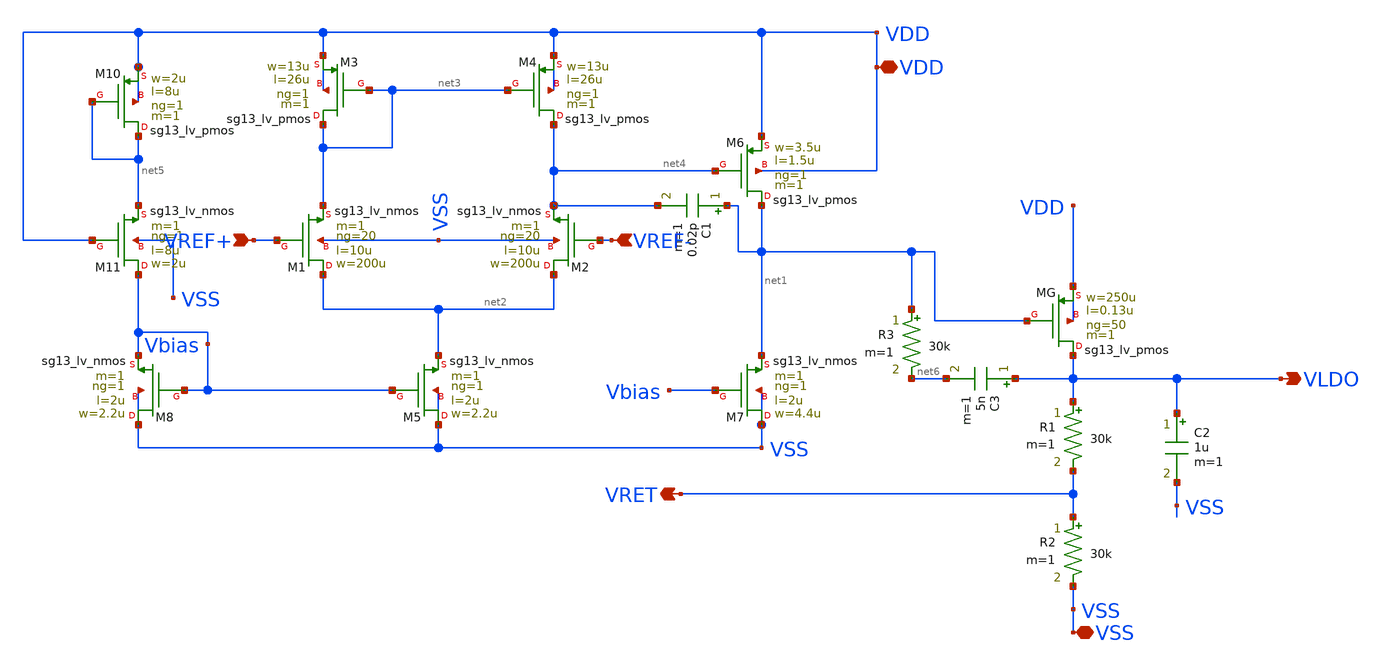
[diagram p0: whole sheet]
** sch_path: designs/1iee34/LDO_PERF.sch
**.subckt LDO_PERF VREF+ VREF- VLDO VSS VDD VRET
*.ipin VREF+
*.ipin VREF-
*.opin VLDO
*.iopin VSS
*.iopin VDD
*.opin VRET
XMG VLDO net1 VDD VDD sg13_lv_pmos w=250u l=0.13u ng=50 m=1 mm_ok=1
R2 VRET VSS 30k m=1
R1 VLDO VRET 30k m=1
XM1 net2 VREF+ net3 VSS sg13_lv_nmos w=200u l=10u ng=20 m=1 mm_ok=1
XM2 net2 VREF- net4 VSS sg13_lv_nmos w=200u l=10u ng=20 m=1 mm_ok=1
XM3 net3 net3 VDD VDD sg13_lv_pmos w=13u l=26u ng=1 m=1 mm_ok=1
XM4 net4 net3 VDD VDD sg13_lv_pmos w=13u l=26u ng=1 m=1 mm_ok=1
XM5 VSS Vbias net2 VSS sg13_lv_nmos w=2.2u l=2u ng=1 m=1 mm_ok=1
XM8 VSS Vbias Vbias VSS sg13_lv_nmos w=2.2u l=2u ng=1 m=1 mm_ok=1
XM7 VSS Vbias net1 VSS sg13_lv_nmos w=4.4u l=2u ng=1 m=1 mm_ok=1
XM6 net1 net4 VDD VDD sg13_lv_pmos w=3.5u l=1.5u ng=1 m=1 mm_ok=1
C1 net1 net4 0.02p m=1
C2 VLDO VSS 1u m=1
XM10 net5 net5 VDD VDD sg13_lv_pmos w=2u l=8u ng=1 m=1 mm_ok=1
XM11 Vbias VDD net5 VSS sg13_lv_nmos w=2u l=8u ng=1 m=1 mm_ok=1
C3 VLDO net6 5n m=1
R3 net1 net6 30k m=1
**.ends
.end
